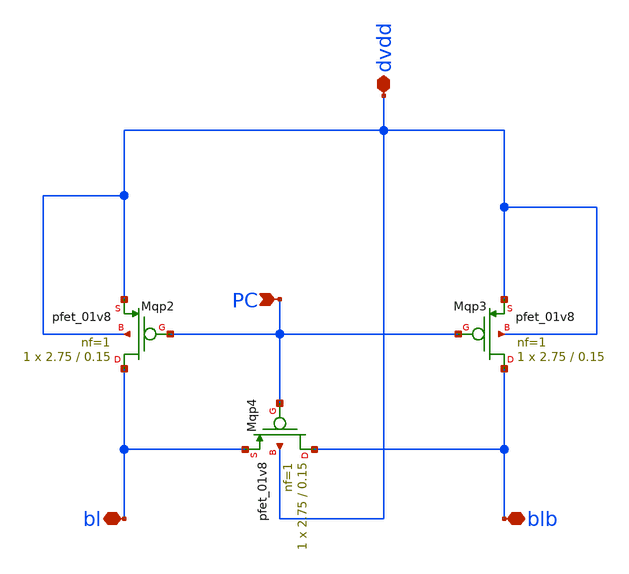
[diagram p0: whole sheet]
** sch_path: pc_ckt.sch
**.subckt pc_ckt blb bl dvdd PC
*.iopin blb
*.iopin bl
*.iopin dvdd
*.ipin PC
XMqp2 bl PC dvdd dvdd sky130_fd_pr__pfet_01v8 L=0.15 W=2.75 nf=1 ad='int((1 + 1)/2) * 2.75 / 1 * 0.29'
+ as='int((1 + 2)/2) * 2.75 / 1 * 0.29' pd='2*int((1 + 1)/2) * (2.75 / 1 + 0.29)' ps='2*int((1 + 2)/2) * (2.75 / 1 + 0.29)'
+ nrd='0.29 / 2.75 ' nrs='0.29 / 2.75 ' sa=0 sb=0 sd=0 mult=1 m=1
XMqp3 blb PC dvdd dvdd sky130_fd_pr__pfet_01v8 L=0.15 W=2.75 nf=1 ad='int((1 + 1)/2) * 2.75 / 1 * 0.29'
+ as='int((1 + 2)/2) * 2.75 / 1 * 0.29' pd='2*int((1 + 1)/2) * (2.75 / 1 + 0.29)' ps='2*int((1 + 2)/2) * (2.75 / 1 + 0.29)'
+ nrd='0.29 / 2.75 ' nrs='0.29 / 2.75 ' sa=0 sb=0 sd=0 mult=1 m=1
XMqp4 blb PC bl dvdd sky130_fd_pr__pfet_01v8 L=0.15 W=2.75 nf=1 ad='int((1 + 1)/2) * 2.75 / 1 * 0.29'
+ as='int((1 + 2)/2) * 2.75 / 1 * 0.29' pd='2*int((1 + 1)/2) * (2.75 / 1 + 0.29)' ps='2*int((1 + 2)/2) * (2.75 / 1 + 0.29)'
+ nrd='0.29 / 2.75 ' nrs='0.29 / 2.75 ' sa=0 sb=0 sd=0 mult=1 m=1
**.ends
.end
